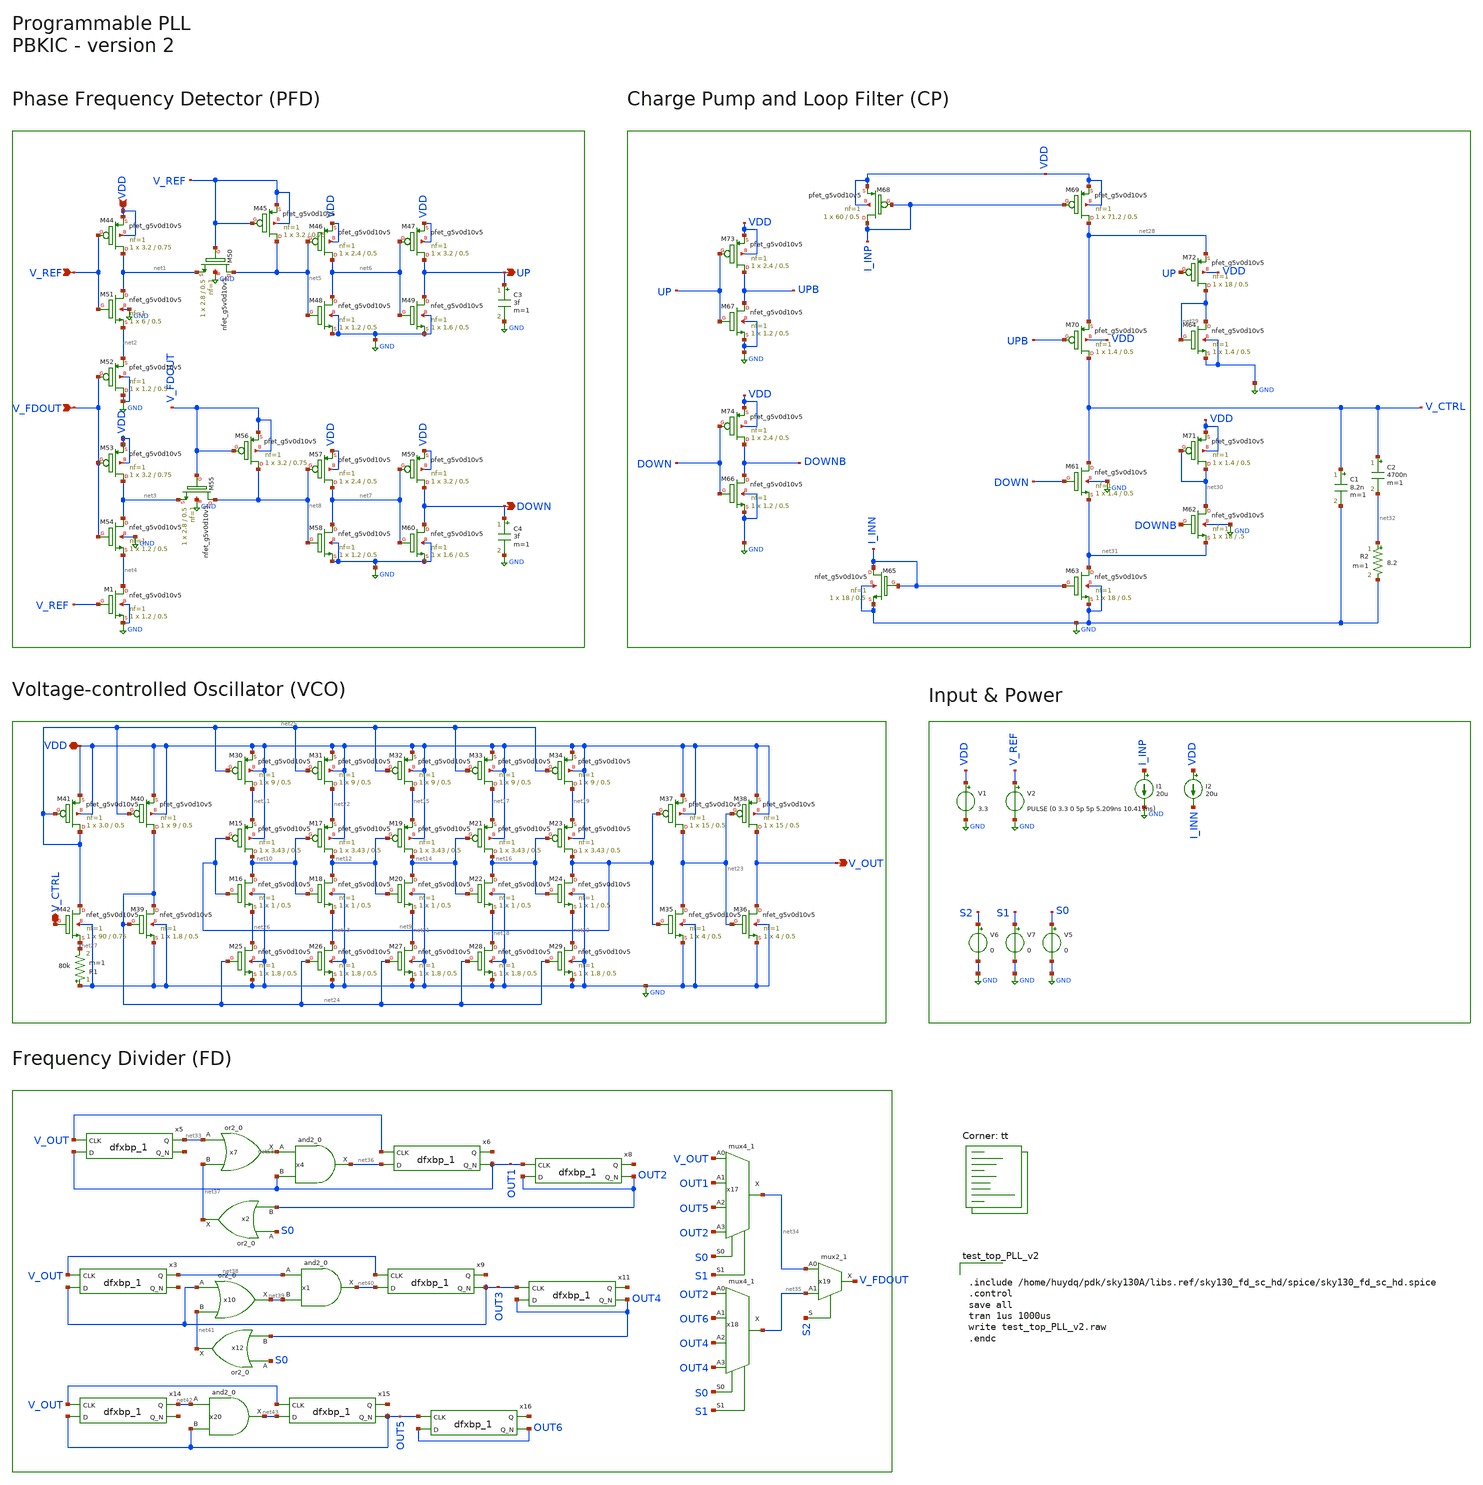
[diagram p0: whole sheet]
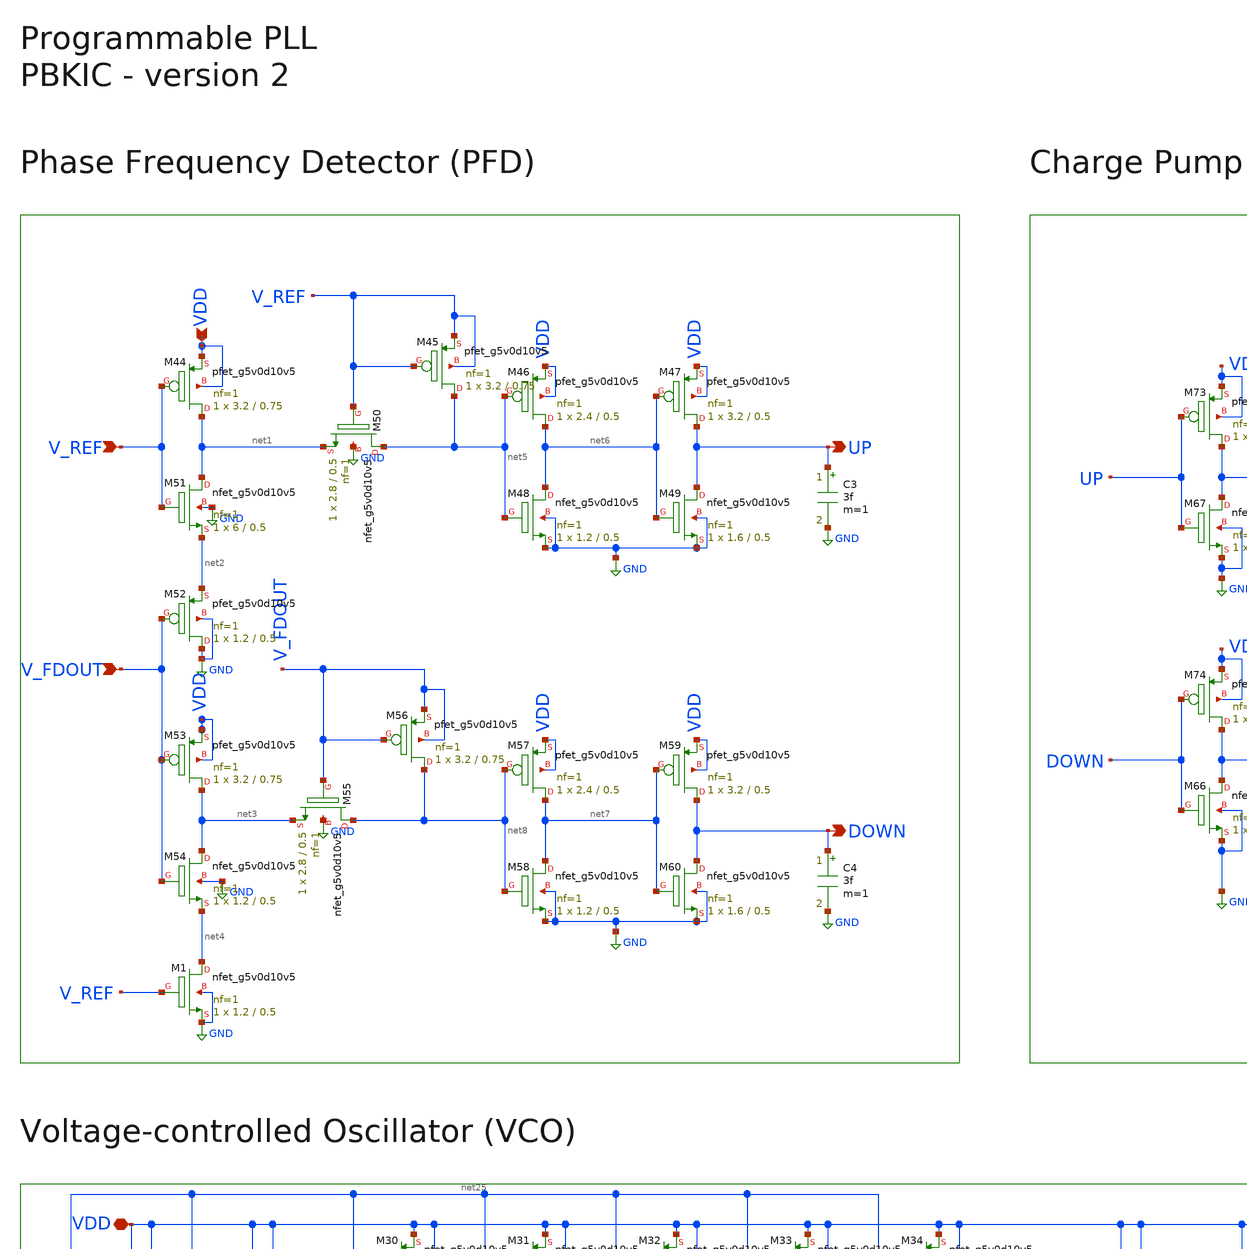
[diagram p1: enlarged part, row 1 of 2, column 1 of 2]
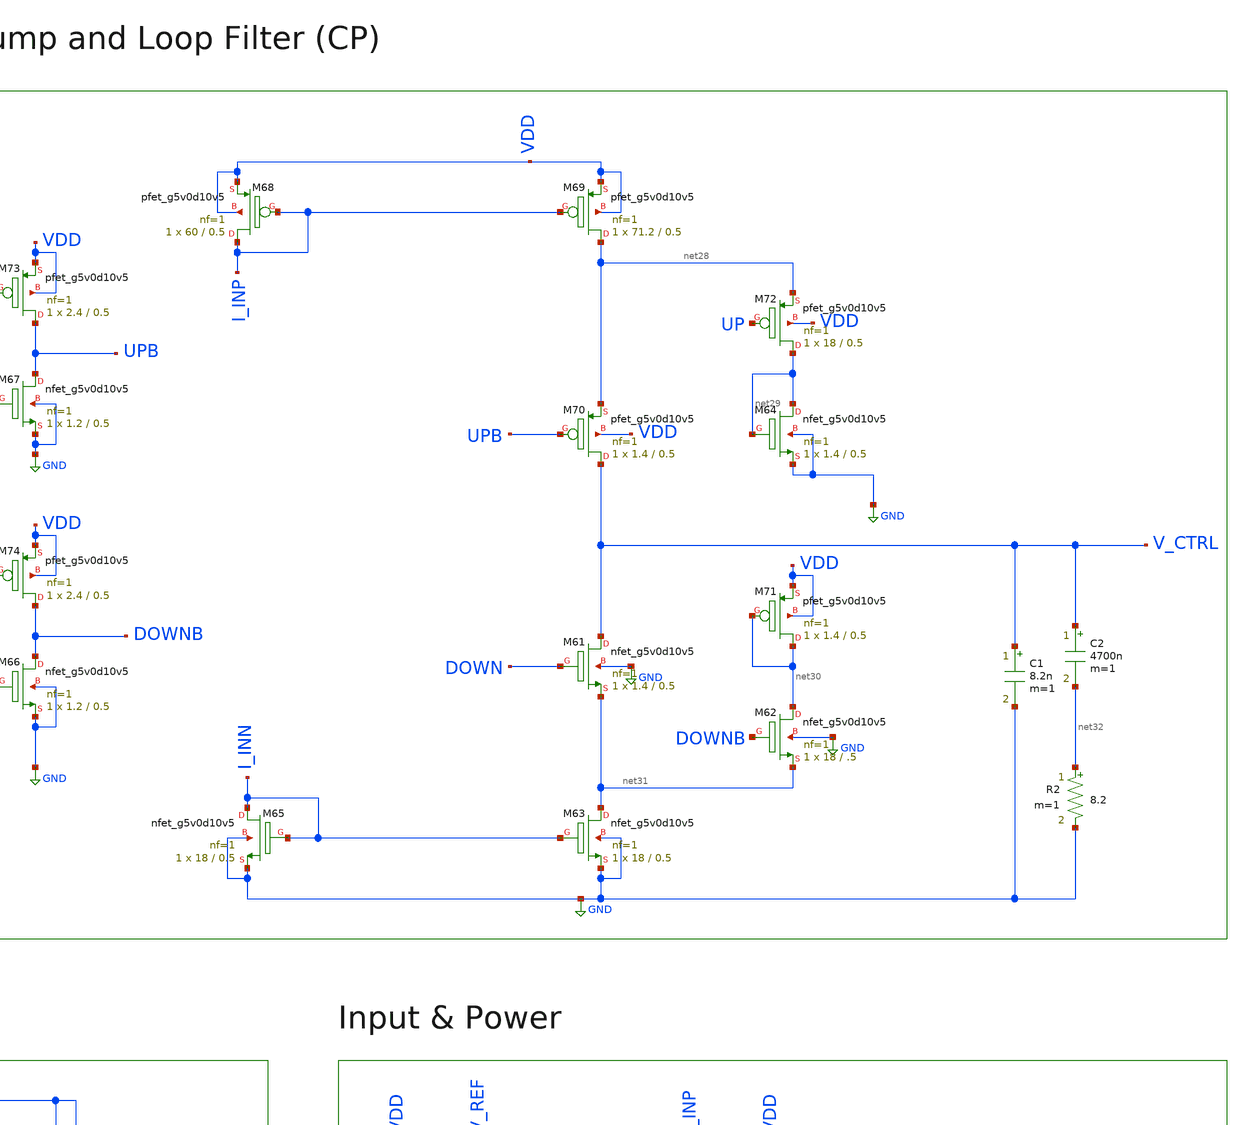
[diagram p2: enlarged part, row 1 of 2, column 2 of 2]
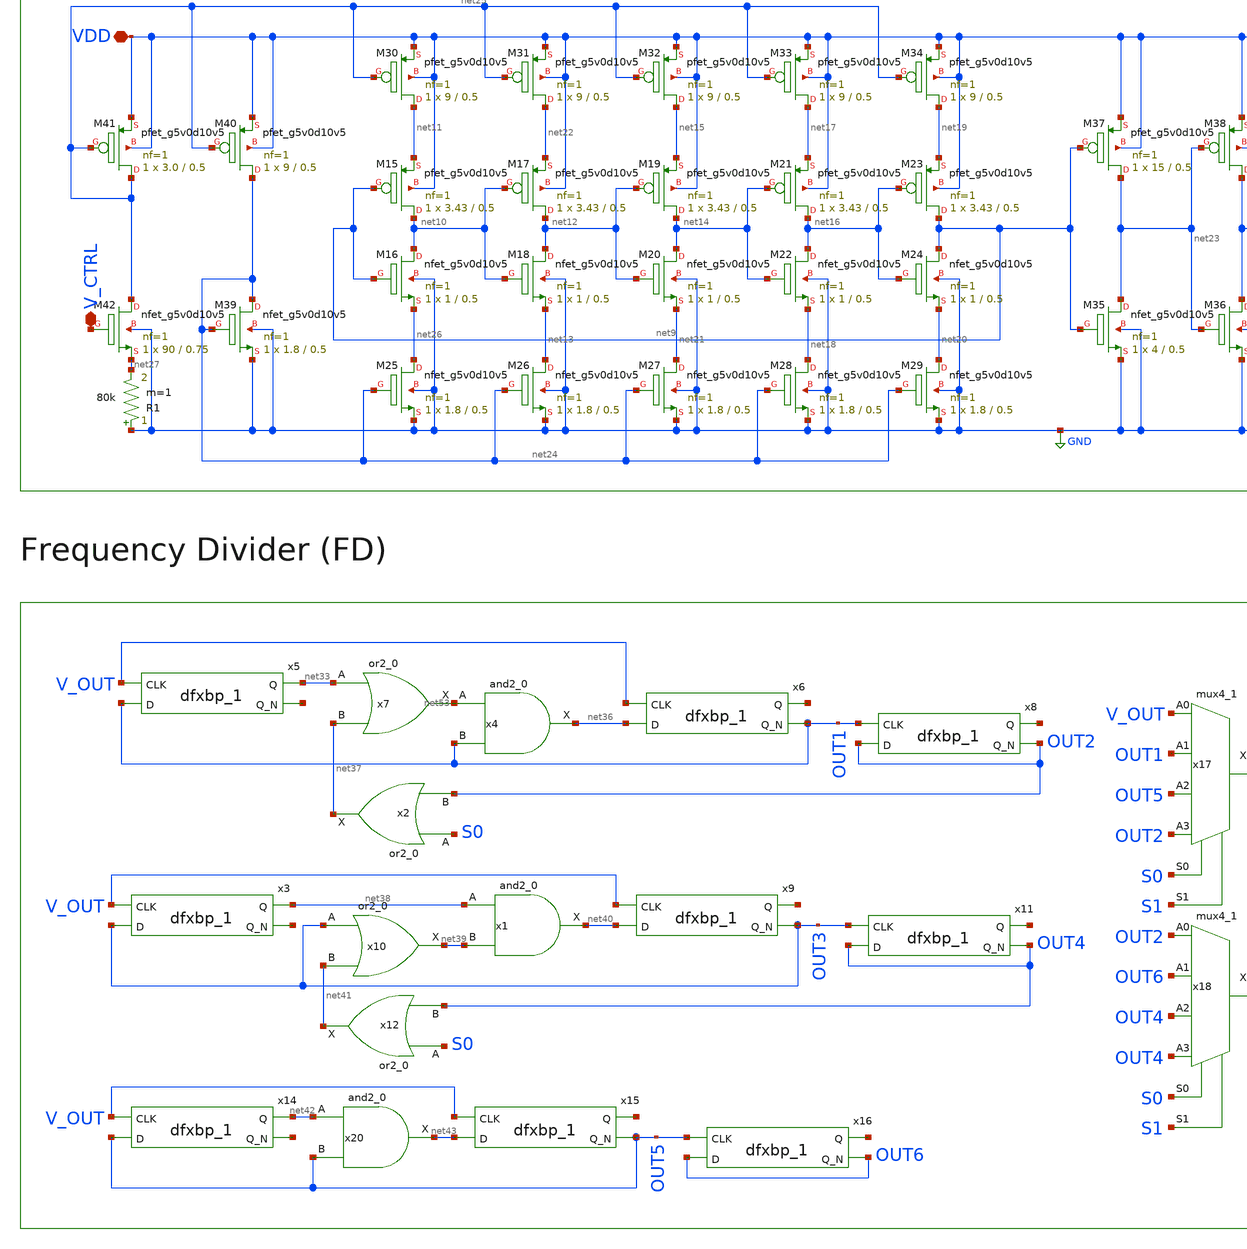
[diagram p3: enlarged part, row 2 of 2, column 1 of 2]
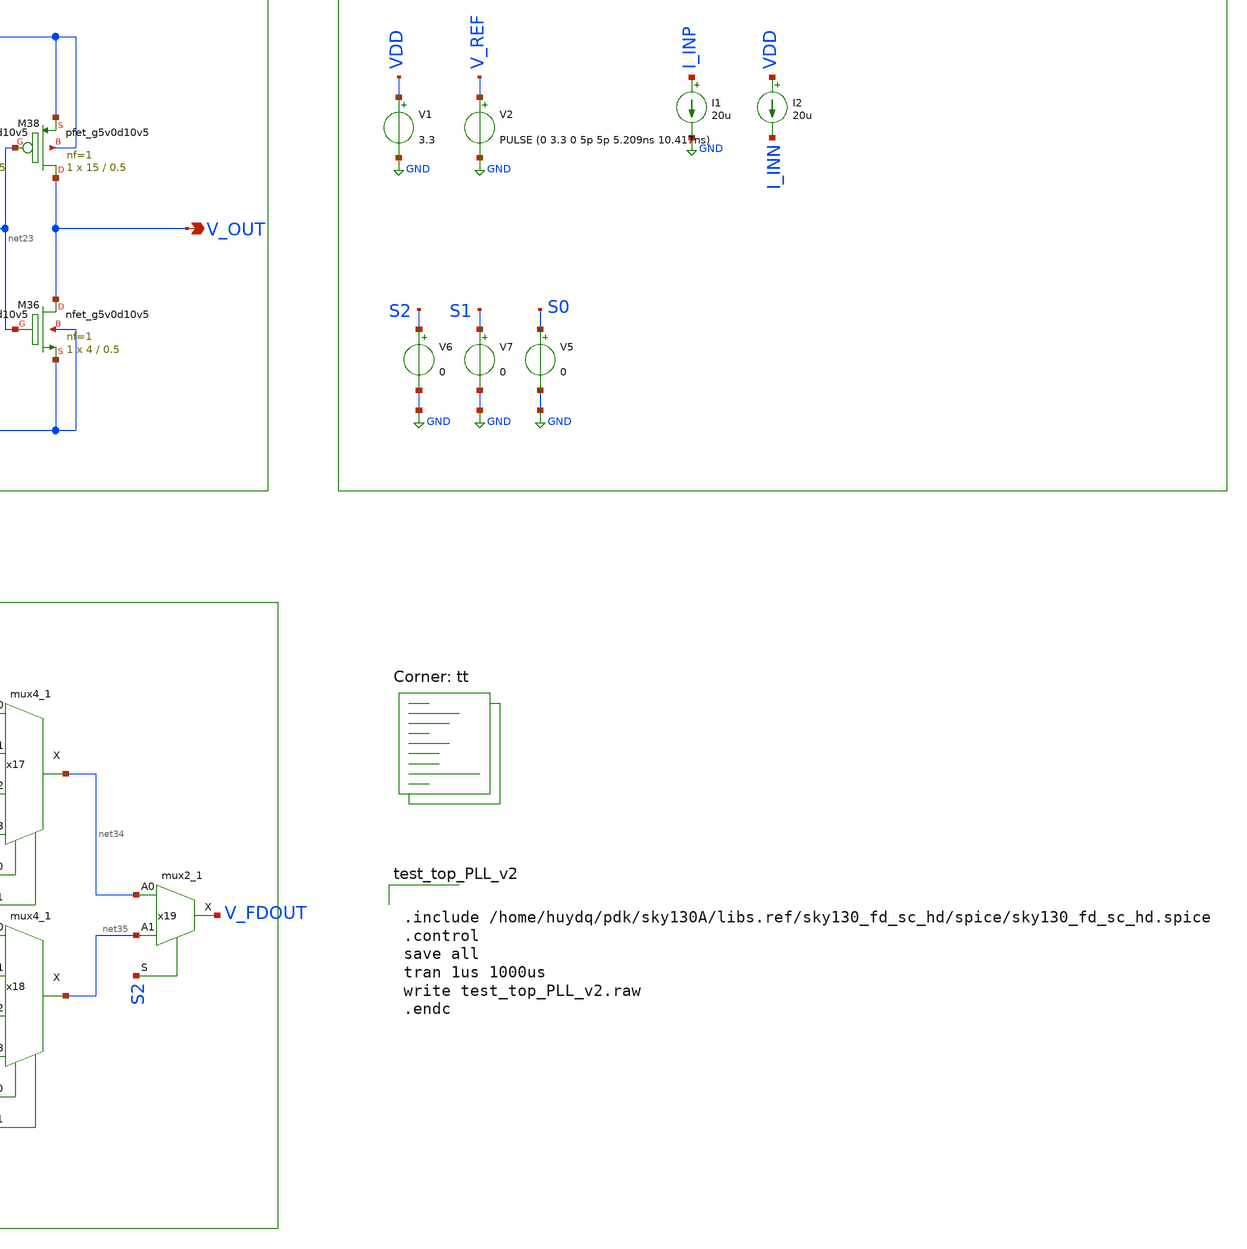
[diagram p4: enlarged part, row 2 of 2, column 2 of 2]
** sch_path: test_top_PLL_v2.sch
**.subckt test_top_PLL_v2 V_REF V_FDOUT DOWN UP VDD VDD V_OUT V_CTRL
*.ipin V_REF
*.ipin V_FDOUT
*.opin DOWN
*.opin UP
*.ipin VDD
*.iopin VDD
*.opin V_OUT
*.iopin V_CTRL
C3 UP GND 3f m=1
C4 DOWN GND 3f m=1
XM44 net1 V_REF VDD VDD sky130_fd_pr__pfet_g5v0d10v5 L=0.75 W=3.2 nf=1 ad='int((nf+1)/2) * W/nf * 0.29'
+ as='int((nf+2)/2) * W/nf * 0.29' pd='2*int((nf+1)/2) * (W/nf + 0.29)' ps='2*int((nf+2)/2) * (W/nf + 0.29)'
+ nrd='0.29 / W' nrs='0.29 / W' sa=0 sb=0 sd=0 mult=1 m=1
XM45 net5 V_REF V_REF V_REF sky130_fd_pr__pfet_g5v0d10v5 L=0.75 W=3.2 nf=1 ad='int((nf+1)/2) * W/nf * 0.29'
+ as='int((nf+2)/2) * W/nf * 0.29' pd='2*int((nf+1)/2) * (W/nf + 0.29)' ps='2*int((nf+2)/2) * (W/nf + 0.29)'
+ nrd='0.29 / W' nrs='0.29 / W' sa=0 sb=0 sd=0 mult=1 m=1
XM46 net6 net5 VDD VDD sky130_fd_pr__pfet_g5v0d10v5 L=0.5 W=2.4 nf=1 ad='int((nf+1)/2) * W/nf * 0.29'
+ as='int((nf+2)/2) * W/nf * 0.29' pd='2*int((nf+1)/2) * (W/nf + 0.29)' ps='2*int((nf+2)/2) * (W/nf + 0.29)'
+ nrd='0.29 / W' nrs='0.29 / W' sa=0 sb=0 sd=0 mult=1 m=1
XM47 UP net6 VDD VDD sky130_fd_pr__pfet_g5v0d10v5 L=0.5 W=3.2 nf=1 ad='int((nf+1)/2) * W/nf * 0.29' as='int((nf+2)/2) * W/nf * 0.29'
+ pd='2*int((nf+1)/2) * (W/nf + 0.29)' ps='2*int((nf+2)/2) * (W/nf + 0.29)' nrd='0.29 / W' nrs='0.29 / W'
+ sa=0 sb=0 sd=0 mult=1 m=1
XM48 net6 net5 GND GND sky130_fd_pr__nfet_g5v0d10v5 L=0.5 W=1.2 nf=1 ad='int((nf+1)/2) * W/nf * 0.29'
+ as='int((nf+2)/2) * W/nf * 0.29' pd='2*int((nf+1)/2) * (W/nf + 0.29)' ps='2*int((nf+2)/2) * (W/nf + 0.29)'
+ nrd='0.29 / W' nrs='0.29 / W' sa=0 sb=0 sd=0 mult=1 m=1
XM49 UP net6 GND GND sky130_fd_pr__nfet_g5v0d10v5 L=0.5 W=1.6 nf=1 ad='int((nf+1)/2) * W/nf * 0.29' as='int((nf+2)/2) * W/nf * 0.29'
+ pd='2*int((nf+1)/2) * (W/nf + 0.29)' ps='2*int((nf+2)/2) * (W/nf + 0.29)' nrd='0.29 / W' nrs='0.29 / W'
+ sa=0 sb=0 sd=0 mult=1 m=1
XM50 net5 V_REF net1 GND sky130_fd_pr__nfet_g5v0d10v5 L=0.5 W=2.8 nf=1 ad='int((nf+1)/2) * W/nf * 0.29'
+ as='int((nf+2)/2) * W/nf * 0.29' pd='2*int((nf+1)/2) * (W/nf + 0.29)' ps='2*int((nf+2)/2) * (W/nf + 0.29)'
+ nrd='0.29 / W' nrs='0.29 / W' sa=0 sb=0 sd=0 mult=1 m=1
XM51 net1 V_REF net2 GND sky130_fd_pr__nfet_g5v0d10v5 L=0.5 W=6 nf=1 ad='int((nf+1)/2) * W/nf * 0.29'
+ as='int((nf+2)/2) * W/nf * 0.29' pd='2*int((nf+1)/2) * (W/nf + 0.29)' ps='2*int((nf+2)/2) * (W/nf + 0.29)'
+ nrd='0.29 / W' nrs='0.29 / W' sa=0 sb=0 sd=0 mult=1 m=1
XM52 GND V_FDOUT net2 GND sky130_fd_pr__pfet_g5v0d10v5 L=0.5 W=1.2 nf=1 ad='int((nf+1)/2) * W/nf * 0.29'
+ as='int((nf+2)/2) * W/nf * 0.29' pd='2*int((nf+1)/2) * (W/nf + 0.29)' ps='2*int((nf+2)/2) * (W/nf + 0.29)'
+ nrd='0.29 / W' nrs='0.29 / W' sa=0 sb=0 sd=0 mult=1 m=1
XM53 net3 V_FDOUT VDD VDD sky130_fd_pr__pfet_g5v0d10v5 L=0.75 W=3.2 nf=1 ad='int((nf+1)/2) * W/nf * 0.29'
+ as='int((nf+2)/2) * W/nf * 0.29' pd='2*int((nf+1)/2) * (W/nf + 0.29)' ps='2*int((nf+2)/2) * (W/nf + 0.29)'
+ nrd='0.29 / W' nrs='0.29 / W' sa=0 sb=0 sd=0 mult=1 m=1
XM54 net3 V_FDOUT net4 GND sky130_fd_pr__nfet_g5v0d10v5 L=0.5 W=1.2 nf=1 ad='int((nf+1)/2) * W/nf * 0.29'
+ as='int((nf+2)/2) * W/nf * 0.29' pd='2*int((nf+1)/2) * (W/nf + 0.29)' ps='2*int((nf+2)/2) * (W/nf + 0.29)'
+ nrd='0.29 / W' nrs='0.29 / W' sa=0 sb=0 sd=0 mult=1 m=1
XM55 net8 V_FDOUT net3 GND sky130_fd_pr__nfet_g5v0d10v5 L=0.5 W=2.8 nf=1 ad='int((nf+1)/2) * W/nf * 0.29'
+ as='int((nf+2)/2) * W/nf * 0.29' pd='2*int((nf+1)/2) * (W/nf + 0.29)' ps='2*int((nf+2)/2) * (W/nf + 0.29)'
+ nrd='0.29 / W' nrs='0.29 / W' sa=0 sb=0 sd=0 mult=1 m=1
XM56 net8 V_FDOUT V_FDOUT V_FDOUT sky130_fd_pr__pfet_g5v0d10v5 L=0.75 W=3.2 nf=1 ad='int((nf+1)/2) * W/nf * 0.29'
+ as='int((nf+2)/2) * W/nf * 0.29' pd='2*int((nf+1)/2) * (W/nf + 0.29)' ps='2*int((nf+2)/2) * (W/nf + 0.29)'
+ nrd='0.29 / W' nrs='0.29 / W' sa=0 sb=0 sd=0 mult=1 m=1
XM57 net7 net8 VDD VDD sky130_fd_pr__pfet_g5v0d10v5 L=0.5 W=2.4 nf=1 ad='int((nf+1)/2) * W/nf * 0.29'
+ as='int((nf+2)/2) * W/nf * 0.29' pd='2*int((nf+1)/2) * (W/nf + 0.29)' ps='2*int((nf+2)/2) * (W/nf + 0.29)'
+ nrd='0.29 / W' nrs='0.29 / W' sa=0 sb=0 sd=0 mult=1 m=1
XM58 net7 net8 GND GND sky130_fd_pr__nfet_g5v0d10v5 L=0.5 W=1.2 nf=1 ad='int((nf+1)/2) * W/nf * 0.29'
+ as='int((nf+2)/2) * W/nf * 0.29' pd='2*int((nf+1)/2) * (W/nf + 0.29)' ps='2*int((nf+2)/2) * (W/nf + 0.29)'
+ nrd='0.29 / W' nrs='0.29 / W' sa=0 sb=0 sd=0 mult=1 m=1
XM59 DOWN net7 VDD VDD sky130_fd_pr__pfet_g5v0d10v5 L=0.5 W=3.2 nf=1 ad='int((nf+1)/2) * W/nf * 0.29'
+ as='int((nf+2)/2) * W/nf * 0.29' pd='2*int((nf+1)/2) * (W/nf + 0.29)' ps='2*int((nf+2)/2) * (W/nf + 0.29)'
+ nrd='0.29 / W' nrs='0.29 / W' sa=0 sb=0 sd=0 mult=1 m=1
XM60 DOWN net7 GND GND sky130_fd_pr__nfet_g5v0d10v5 L=0.5 W=1.6 nf=1 ad='int((nf+1)/2) * W/nf * 0.29'
+ as='int((nf+2)/2) * W/nf * 0.29' pd='2*int((nf+1)/2) * (W/nf + 0.29)' ps='2*int((nf+2)/2) * (W/nf + 0.29)'
+ nrd='0.29 / W' nrs='0.29 / W' sa=0 sb=0 sd=0 mult=1 m=1
XM15 net10 net9 net11 VDD sky130_fd_pr__pfet_g5v0d10v5 L=0.5 W=3.43 nf=1 ad='int((nf+1)/2) * W/nf * 0.29'
+ as='int((nf+2)/2) * W/nf * 0.29' pd='2*int((nf+1)/2) * (W/nf + 0.29)' ps='2*int((nf+2)/2) * (W/nf + 0.29)'
+ nrd='0.29 / W' nrs='0.29 / W' sa=0 sb=0 sd=0 mult=1 m=1
XM16 net10 net9 net26 GND sky130_fd_pr__nfet_g5v0d10v5 L=0.5 W=1 nf=1 ad='int((nf+1)/2) * W/nf * 0.29'
+ as='int((nf+2)/2) * W/nf * 0.29' pd='2*int((nf+1)/2) * (W/nf + 0.29)' ps='2*int((nf+2)/2) * (W/nf + 0.29)'
+ nrd='0.29 / W' nrs='0.29 / W' sa=0 sb=0 sd=0 mult=1 m=1
XM17 net12 net10 net22 VDD sky130_fd_pr__pfet_g5v0d10v5 L=0.5 W=3.43 nf=1 ad='int((nf+1)/2) * W/nf * 0.29'
+ as='int((nf+2)/2) * W/nf * 0.29' pd='2*int((nf+1)/2) * (W/nf + 0.29)' ps='2*int((nf+2)/2) * (W/nf + 0.29)'
+ nrd='0.29 / W' nrs='0.29 / W' sa=0 sb=0 sd=0 mult=1 m=1
XM18 net12 net10 net13 GND sky130_fd_pr__nfet_g5v0d10v5 L=0.5 W=1 nf=1 ad='int((nf+1)/2) * W/nf * 0.29'
+ as='int((nf+2)/2) * W/nf * 0.29' pd='2*int((nf+1)/2) * (W/nf + 0.29)' ps='2*int((nf+2)/2) * (W/nf + 0.29)'
+ nrd='0.29 / W' nrs='0.29 / W' sa=0 sb=0 sd=0 mult=1 m=1
XM19 net14 net12 net15 VDD sky130_fd_pr__pfet_g5v0d10v5 L=0.5 W=3.43 nf=1 ad='int((nf+1)/2) * W/nf * 0.29'
+ as='int((nf+2)/2) * W/nf * 0.29' pd='2*int((nf+1)/2) * (W/nf + 0.29)' ps='2*int((nf+2)/2) * (W/nf + 0.29)'
+ nrd='0.29 / W' nrs='0.29 / W' sa=0 sb=0 sd=0 mult=1 m=1
XM20 net14 net12 net21 GND sky130_fd_pr__nfet_g5v0d10v5 L=0.5 W=1 nf=1 ad='int((nf+1)/2) * W/nf * 0.29'
+ as='int((nf+2)/2) * W/nf * 0.29' pd='2*int((nf+1)/2) * (W/nf + 0.29)' ps='2*int((nf+2)/2) * (W/nf + 0.29)'
+ nrd='0.29 / W' nrs='0.29 / W' sa=0 sb=0 sd=0 mult=1 m=1
XM21 net16 net14 net17 VDD sky130_fd_pr__pfet_g5v0d10v5 L=0.5 W=3.43 nf=1 ad='int((nf+1)/2) * W/nf * 0.29'
+ as='int((nf+2)/2) * W/nf * 0.29' pd='2*int((nf+1)/2) * (W/nf + 0.29)' ps='2*int((nf+2)/2) * (W/nf + 0.29)'
+ nrd='0.29 / W' nrs='0.29 / W' sa=0 sb=0 sd=0 mult=1 m=1
XM22 net16 net14 net18 GND sky130_fd_pr__nfet_g5v0d10v5 L=0.5 W=1 nf=1 ad='int((nf+1)/2) * W/nf * 0.29'
+ as='int((nf+2)/2) * W/nf * 0.29' pd='2*int((nf+1)/2) * (W/nf + 0.29)' ps='2*int((nf+2)/2) * (W/nf + 0.29)'
+ nrd='0.29 / W' nrs='0.29 / W' sa=0 sb=0 sd=0 mult=1 m=1
XM23 net9 net16 net19 VDD sky130_fd_pr__pfet_g5v0d10v5 L=0.5 W=3.43 nf=1 ad='int((nf+1)/2) * W/nf * 0.29'
+ as='int((nf+2)/2) * W/nf * 0.29' pd='2*int((nf+1)/2) * (W/nf + 0.29)' ps='2*int((nf+2)/2) * (W/nf + 0.29)'
+ nrd='0.29 / W' nrs='0.29 / W' sa=0 sb=0 sd=0 mult=1 m=1
XM24 net9 net16 net20 GND sky130_fd_pr__nfet_g5v0d10v5 L=0.5 W=1 nf=1 ad='int((nf+1)/2) * W/nf * 0.29'
+ as='int((nf+2)/2) * W/nf * 0.29' pd='2*int((nf+1)/2) * (W/nf + 0.29)' ps='2*int((nf+2)/2) * (W/nf + 0.29)'
+ nrd='0.29 / W' nrs='0.29 / W' sa=0 sb=0 sd=0 mult=1 m=1
XM25 net26 net24 GND GND sky130_fd_pr__nfet_g5v0d10v5 L=0.5 W=1.8 nf=1 ad='int((nf+1)/2) * W/nf * 0.29'
+ as='int((nf+2)/2) * W/nf * 0.29' pd='2*int((nf+1)/2) * (W/nf + 0.29)' ps='2*int((nf+2)/2) * (W/nf + 0.29)'
+ nrd='0.29 / W' nrs='0.29 / W' sa=0 sb=0 sd=0 mult=1 m=1
XM26 net13 net24 GND GND sky130_fd_pr__nfet_g5v0d10v5 L=0.5 W=1.8 nf=1 ad='int((nf+1)/2) * W/nf * 0.29'
+ as='int((nf+2)/2) * W/nf * 0.29' pd='2*int((nf+1)/2) * (W/nf + 0.29)' ps='2*int((nf+2)/2) * (W/nf + 0.29)'
+ nrd='0.29 / W' nrs='0.29 / W' sa=0 sb=0 sd=0 mult=1 m=1
XM27 net21 net24 GND GND sky130_fd_pr__nfet_g5v0d10v5 L=0.5 W=1.8 nf=1 ad='int((nf+1)/2) * W/nf * 0.29'
+ as='int((nf+2)/2) * W/nf * 0.29' pd='2*int((nf+1)/2) * (W/nf + 0.29)' ps='2*int((nf+2)/2) * (W/nf + 0.29)'
+ nrd='0.29 / W' nrs='0.29 / W' sa=0 sb=0 sd=0 mult=1 m=1
XM28 net18 net24 GND GND sky130_fd_pr__nfet_g5v0d10v5 L=0.5 W=1.8 nf=1 ad='int((nf+1)/2) * W/nf * 0.29'
+ as='int((nf+2)/2) * W/nf * 0.29' pd='2*int((nf+1)/2) * (W/nf + 0.29)' ps='2*int((nf+2)/2) * (W/nf + 0.29)'
+ nrd='0.29 / W' nrs='0.29 / W' sa=0 sb=0 sd=0 mult=1 m=1
XM29 net20 net24 GND GND sky130_fd_pr__nfet_g5v0d10v5 L=0.5 W=1.8 nf=1 ad='int((nf+1)/2) * W/nf * 0.29'
+ as='int((nf+2)/2) * W/nf * 0.29' pd='2*int((nf+1)/2) * (W/nf + 0.29)' ps='2*int((nf+2)/2) * (W/nf + 0.29)'
+ nrd='0.29 / W' nrs='0.29 / W' sa=0 sb=0 sd=0 mult=1 m=1
XM30 net11 net25 VDD VDD sky130_fd_pr__pfet_g5v0d10v5 L=0.5 W=9 nf=1 ad='int((nf+1)/2) * W/nf * 0.29'
+ as='int((nf+2)/2) * W/nf * 0.29' pd='2*int((nf+1)/2) * (W/nf + 0.29)' ps='2*int((nf+2)/2) * (W/nf + 0.29)'
+ nrd='0.29 / W' nrs='0.29 / W' sa=0 sb=0 sd=0 mult=1 m=1
XM31 net22 net25 VDD VDD sky130_fd_pr__pfet_g5v0d10v5 L=0.5 W=9 nf=1 ad='int((nf+1)/2) * W/nf * 0.29'
+ as='int((nf+2)/2) * W/nf * 0.29' pd='2*int((nf+1)/2) * (W/nf + 0.29)' ps='2*int((nf+2)/2) * (W/nf + 0.29)'
+ nrd='0.29 / W' nrs='0.29 / W' sa=0 sb=0 sd=0 mult=1 m=1
XM32 net15 net25 VDD VDD sky130_fd_pr__pfet_g5v0d10v5 L=0.5 W=9 nf=1 ad='int((nf+1)/2) * W/nf * 0.29'
+ as='int((nf+2)/2) * W/nf * 0.29' pd='2*int((nf+1)/2) * (W/nf + 0.29)' ps='2*int((nf+2)/2) * (W/nf + 0.29)'
+ nrd='0.29 / W' nrs='0.29 / W' sa=0 sb=0 sd=0 mult=1 m=1
XM33 net17 net25 VDD VDD sky130_fd_pr__pfet_g5v0d10v5 L=0.5 W=9 nf=1 ad='int((nf+1)/2) * W/nf * 0.29'
+ as='int((nf+2)/2) * W/nf * 0.29' pd='2*int((nf+1)/2) * (W/nf + 0.29)' ps='2*int((nf+2)/2) * (W/nf + 0.29)'
+ nrd='0.29 / W' nrs='0.29 / W' sa=0 sb=0 sd=0 mult=1 m=1
XM34 net19 net25 VDD VDD sky130_fd_pr__pfet_g5v0d10v5 L=0.5 W=9 nf=1 ad='int((nf+1)/2) * W/nf * 0.29'
+ as='int((nf+2)/2) * W/nf * 0.29' pd='2*int((nf+1)/2) * (W/nf + 0.29)' ps='2*int((nf+2)/2) * (W/nf + 0.29)'
+ nrd='0.29 / W' nrs='0.29 / W' sa=0 sb=0 sd=0 mult=1 m=1
XM35 net23 net9 GND GND sky130_fd_pr__nfet_g5v0d10v5 L=0.5 W=4 nf=1 ad='int((nf+1)/2) * W/nf * 0.29'
+ as='int((nf+2)/2) * W/nf * 0.29' pd='2*int((nf+1)/2) * (W/nf + 0.29)' ps='2*int((nf+2)/2) * (W/nf + 0.29)'
+ nrd='0.29 / W' nrs='0.29 / W' sa=0 sb=0 sd=0 mult=1 m=1
XM36 V_OUT net23 GND GND sky130_fd_pr__nfet_g5v0d10v5 L=0.5 W=4 nf=1 ad='int((nf+1)/2) * W/nf * 0.29'
+ as='int((nf+2)/2) * W/nf * 0.29' pd='2*int((nf+1)/2) * (W/nf + 0.29)' ps='2*int((nf+2)/2) * (W/nf + 0.29)'
+ nrd='0.29 / W' nrs='0.29 / W' sa=0 sb=0 sd=0 mult=1 m=1
XM37 net23 net9 VDD VDD sky130_fd_pr__pfet_g5v0d10v5 L=0.5 W=15 nf=1 ad='int((nf+1)/2) * W/nf * 0.29'
+ as='int((nf+2)/2) * W/nf * 0.29' pd='2*int((nf+1)/2) * (W/nf + 0.29)' ps='2*int((nf+2)/2) * (W/nf + 0.29)'
+ nrd='0.29 / W' nrs='0.29 / W' sa=0 sb=0 sd=0 mult=1 m=1
XM38 V_OUT net23 VDD VDD sky130_fd_pr__pfet_g5v0d10v5 L=0.5 W=15 nf=1 ad='int((nf+1)/2) * W/nf * 0.29'
+ as='int((nf+2)/2) * W/nf * 0.29' pd='2*int((nf+1)/2) * (W/nf + 0.29)' ps='2*int((nf+2)/2) * (W/nf + 0.29)'
+ nrd='0.29 / W' nrs='0.29 / W' sa=0 sb=0 sd=0 mult=1 m=1
XM39 net24 net24 GND GND sky130_fd_pr__nfet_g5v0d10v5 L=0.5 W=1.8 nf=1 ad='int((nf+1)/2) * W/nf * 0.29'
+ as='int((nf+2)/2) * W/nf * 0.29' pd='2*int((nf+1)/2) * (W/nf + 0.29)' ps='2*int((nf+2)/2) * (W/nf + 0.29)'
+ nrd='0.29 / W' nrs='0.29 / W' sa=0 sb=0 sd=0 mult=1 m=1
XM40 net24 net25 VDD VDD sky130_fd_pr__pfet_g5v0d10v5 L=0.5 W=9 nf=1 ad='int((nf+1)/2) * W/nf * 0.29'
+ as='int((nf+2)/2) * W/nf * 0.29' pd='2*int((nf+1)/2) * (W/nf + 0.29)' ps='2*int((nf+2)/2) * (W/nf + 0.29)'
+ nrd='0.29 / W' nrs='0.29 / W' sa=0 sb=0 sd=0 mult=1 m=1
XM41 net25 net25 VDD VDD sky130_fd_pr__pfet_g5v0d10v5 L=0.5 W=3.0 nf=1 ad='int((nf+1)/2) * W/nf * 0.29'
+ as='int((nf+2)/2) * W/nf * 0.29' pd='2*int((nf+1)/2) * (W/nf + 0.29)' ps='2*int((nf+2)/2) * (W/nf + 0.29)'
+ nrd='0.29 / W' nrs='0.29 / W' sa=0 sb=0 sd=0 mult=1 m=1
XM42 net25 V_CTRL net27 GND sky130_fd_pr__nfet_g5v0d10v5 L=0.75 W=90 nf=1 ad='int((nf+1)/2) * W/nf * 0.29'
+ as='int((nf+2)/2) * W/nf * 0.29' pd='2*int((nf+1)/2) * (W/nf + 0.29)' ps='2*int((nf+2)/2) * (W/nf + 0.29)'
+ nrd='0.29 / W' nrs='0.29 / W' sa=0 sb=0 sd=0 mult=1 m=1
R1 GND net27 80k m=1
V1 VDD GND 3.3
V2 V_REF GND PULSE (0 3.3 0 5p 5p 5.209ns 10.417ns)
XM61 V_CTRL DOWN net31 GND sky130_fd_pr__nfet_g5v0d10v5 L=0.5 W=1.4 nf=1 ad='int((nf+1)/2) * W/nf * 0.29'
+ as='int((nf+2)/2) * W/nf * 0.29' pd='2*int((nf+1)/2) * (W/nf + 0.29)' ps='2*int((nf+2)/2) * (W/nf + 0.29)'
+ nrd='0.29 / W' nrs='0.29 / W' sa=0 sb=0 sd=0 mult=1 m=1
XM62 net30 DOWNB net31 GND sky130_fd_pr__nfet_g5v0d10v5 L=.5 W=18 nf=1 ad='int((nf+1)/2) * W/nf * 0.29'
+ as='int((nf+2)/2) * W/nf * 0.29' pd='2*int((nf+1)/2) * (W/nf + 0.29)' ps='2*int((nf+2)/2) * (W/nf + 0.29)'
+ nrd='0.29 / W' nrs='0.29 / W' sa=0 sb=0 sd=0 mult=1 m=1
XM63 net31 I_INN GND GND sky130_fd_pr__nfet_g5v0d10v5 L=0.5 W=18 nf=1 ad='int((nf+1)/2) * W/nf * 0.29'
+ as='int((nf+2)/2) * W/nf * 0.29' pd='2*int((nf+1)/2) * (W/nf + 0.29)' ps='2*int((nf+2)/2) * (W/nf + 0.29)'
+ nrd='0.29 / W' nrs='0.29 / W' sa=0 sb=0 sd=0 mult=1 m=1
XM64 net29 net29 GND GND sky130_fd_pr__nfet_g5v0d10v5 L=0.5 W=1.4 nf=1 ad='int((nf+1)/2) * W/nf * 0.29'
+ as='int((nf+2)/2) * W/nf * 0.29' pd='2*int((nf+1)/2) * (W/nf + 0.29)' ps='2*int((nf+2)/2) * (W/nf + 0.29)'
+ nrd='0.29 / W' nrs='0.29 / W' sa=0 sb=0 sd=0 mult=1 m=1
XM65 I_INN I_INN GND GND sky130_fd_pr__nfet_g5v0d10v5 L=0.5 W=18 nf=1 ad='int((nf+1)/2) * W/nf * 0.29'
+ as='int((nf+2)/2) * W/nf * 0.29' pd='2*int((nf+1)/2) * (W/nf + 0.29)' ps='2*int((nf+2)/2) * (W/nf + 0.29)'
+ nrd='0.29 / W' nrs='0.29 / W' sa=0 sb=0 sd=0 mult=1 m=1
XM66 DOWNB DOWN GND GND sky130_fd_pr__nfet_g5v0d10v5 L=0.5 W=1.2 nf=1 ad='int((nf+1)/2) * W/nf * 0.29'
+ as='int((nf+2)/2) * W/nf * 0.29' pd='2*int((nf+1)/2) * (W/nf + 0.29)' ps='2*int((nf+2)/2) * (W/nf + 0.29)'
+ nrd='0.29 / W' nrs='0.29 / W' sa=0 sb=0 sd=0 mult=1 m=1
XM67 UPB UP GND GND sky130_fd_pr__nfet_g5v0d10v5 L=0.5 W=1.2 nf=1 ad='int((nf+1)/2) * W/nf * 0.29' as='int((nf+2)/2) * W/nf * 0.29'
+ pd='2*int((nf+1)/2) * (W/nf + 0.29)' ps='2*int((nf+2)/2) * (W/nf + 0.29)' nrd='0.29 / W' nrs='0.29 / W'
+ sa=0 sb=0 sd=0 mult=1 m=1
XM68 I_INP I_INP VDD VDD sky130_fd_pr__pfet_g5v0d10v5 L=0.5 W=60 nf=1 ad='int((nf+1)/2) * W/nf * 0.29'
+ as='int((nf+2)/2) * W/nf * 0.29' pd='2*int((nf+1)/2) * (W/nf + 0.29)' ps='2*int((nf+2)/2) * (W/nf + 0.29)'
+ nrd='0.29 / W' nrs='0.29 / W' sa=0 sb=0 sd=0 mult=1 m=1
XM69 net28 I_INP VDD VDD sky130_fd_pr__pfet_g5v0d10v5 L=0.5 W=71.2 nf=1 ad='int((nf+1)/2) * W/nf * 0.29'
+ as='int((nf+2)/2) * W/nf * 0.29' pd='2*int((nf+1)/2) * (W/nf + 0.29)' ps='2*int((nf+2)/2) * (W/nf + 0.29)'
+ nrd='0.29 / W' nrs='0.29 / W' sa=0 sb=0 sd=0 mult=1 m=1
XM70 V_CTRL UPB net28 VDD sky130_fd_pr__pfet_g5v0d10v5 L=0.5 W=1.4 nf=1 ad='int((nf+1)/2) * W/nf * 0.29'
+ as='int((nf+2)/2) * W/nf * 0.29' pd='2*int((nf+1)/2) * (W/nf + 0.29)' ps='2*int((nf+2)/2) * (W/nf + 0.29)'
+ nrd='0.29 / W' nrs='0.29 / W' sa=0 sb=0 sd=0 mult=1 m=1
XM71 net30 net30 VDD VDD sky130_fd_pr__pfet_g5v0d10v5 L=0.5 W=1.4 nf=1 ad='int((nf+1)/2) * W/nf * 0.29'
+ as='int((nf+2)/2) * W/nf * 0.29' pd='2*int((nf+1)/2) * (W/nf + 0.29)' ps='2*int((nf+2)/2) * (W/nf + 0.29)'
+ nrd='0.29 / W' nrs='0.29 / W' sa=0 sb=0 sd=0 mult=1 m=1
XM72 net29 UP net28 VDD sky130_fd_pr__pfet_g5v0d10v5 L=0.5 W=18 nf=1 ad='int((nf+1)/2) * W/nf * 0.29'
+ as='int((nf+2)/2) * W/nf * 0.29' pd='2*int((nf+1)/2) * (W/nf + 0.29)' ps='2*int((nf+2)/2) * (W/nf + 0.29)'
+ nrd='0.29 / W' nrs='0.29 / W' sa=0 sb=0 sd=0 mult=1 m=1
XM73 UPB UP VDD VDD sky130_fd_pr__pfet_g5v0d10v5 L=0.5 W=2.4 nf=1 ad='int((nf+1)/2) * W/nf * 0.29' as='int((nf+2)/2) * W/nf * 0.29'
+ pd='2*int((nf+1)/2) * (W/nf + 0.29)' ps='2*int((nf+2)/2) * (W/nf + 0.29)' nrd='0.29 / W' nrs='0.29 / W'
+ sa=0 sb=0 sd=0 mult=1 m=1
XM74 DOWNB DOWN VDD VDD sky130_fd_pr__pfet_g5v0d10v5 L=0.5 W=2.4 nf=1 ad='int((nf+1)/2) * W/nf * 0.29'
+ as='int((nf+2)/2) * W/nf * 0.29' pd='2*int((nf+1)/2) * (W/nf + 0.29)' ps='2*int((nf+2)/2) * (W/nf + 0.29)'
+ nrd='0.29 / W' nrs='0.29 / W' sa=0 sb=0 sd=0 mult=1 m=1
I2 VDD I_INN 20u
C1 V_CTRL GND 8.2n m=1
C2 V_CTRL net32 4700n m=1
R2 net32 GND 8.2 m=1
I1 I_INP GND 20u
x5 V_OUT OUT1 GND GND VDD VDD net33 net44 sky130_fd_sc_hd__dfxbp_1
x6 V_OUT net36 GND GND VDD VDD net45 OUT1 sky130_fd_sc_hd__dfxbp_1
x8 OUT1 OUT2 GND GND VDD VDD net46 OUT2 sky130_fd_sc_hd__dfxbp_1
x3 V_OUT OUT3 GND GND VDD VDD net38 net47 sky130_fd_sc_hd__dfxbp_1
x9 V_OUT net40 GND GND VDD VDD net48 OUT3 sky130_fd_sc_hd__dfxbp_1
x11 OUT3 OUT4 GND GND VDD VDD net49 OUT4 sky130_fd_sc_hd__dfxbp_1
x14 V_OUT OUT5 GND GND VDD VDD net42 net50 sky130_fd_sc_hd__dfxbp_1
x15 V_OUT net43 GND GND VDD VDD net51 OUT5 sky130_fd_sc_hd__dfxbp_1
x16 OUT5 OUT6 GND GND VDD VDD net52 OUT6 sky130_fd_sc_hd__dfxbp_1
x17 V_OUT OUT1 OUT5 OUT2 S0 S1 GND GND VDD VDD net34 sky130_fd_sc_hd__mux4_1
x18 OUT2 OUT6 OUT4 OUT4 S0 S1 GND GND VDD VDD net35 sky130_fd_sc_hd__mux4_1
x19 net34 net35 S2 GND GND VDD VDD V_FDOUT sky130_fd_sc_hd__mux2_1
x20 net42 OUT5 GND GND VDD VDD net43 sky130_fd_sc_hd__and2_0
x7 net33 net37 GND GND VDD VDD net53 sky130_fd_sc_hd__or2_0
x4 net53 OUT1 GND GND VDD VDD net36 sky130_fd_sc_hd__and2_0
x2 S0 OUT2 GND GND VDD VDD net37 sky130_fd_sc_hd__or2_0
x10 OUT3 net41 GND GND VDD VDD net39 sky130_fd_sc_hd__or2_0
x12 S0 OUT4 GND GND VDD VDD net41 sky130_fd_sc_hd__or2_0
x1 net38 net39 GND GND VDD VDD net40 sky130_fd_sc_hd__and2_0
V5 S0 GND 0
V6 S2 GND 0
V7 S1 GND 0
XM1 net4 V_REF GND GND sky130_fd_pr__nfet_g5v0d10v5 L=0.5 W=1.2 nf=1 ad='int((nf+1)/2) * W/nf * 0.29'
+ as='int((nf+2)/2) * W/nf * 0.29' pd='2*int((nf+1)/2) * (W/nf + 0.29)' ps='2*int((nf+2)/2) * (W/nf + 0.29)'
+ nrd='0.29 / W' nrs='0.29 / W' sa=0 sb=0 sd=0 mult=1 m=1
**** begin user architecture code


.include /home/huydq/pdk/sky130A/libs.ref/sky130_fd_sc_hd/spice/sky130_fd_sc_hd.spice
.control
save all
tran 1us 1000us
write test_top_PLL_v2.raw
.endc

.lib $::SKYWATER_MODELS/sky130.lib.spice tt
**** end user architecture code
**.ends
.GLOBAL GND
.end
